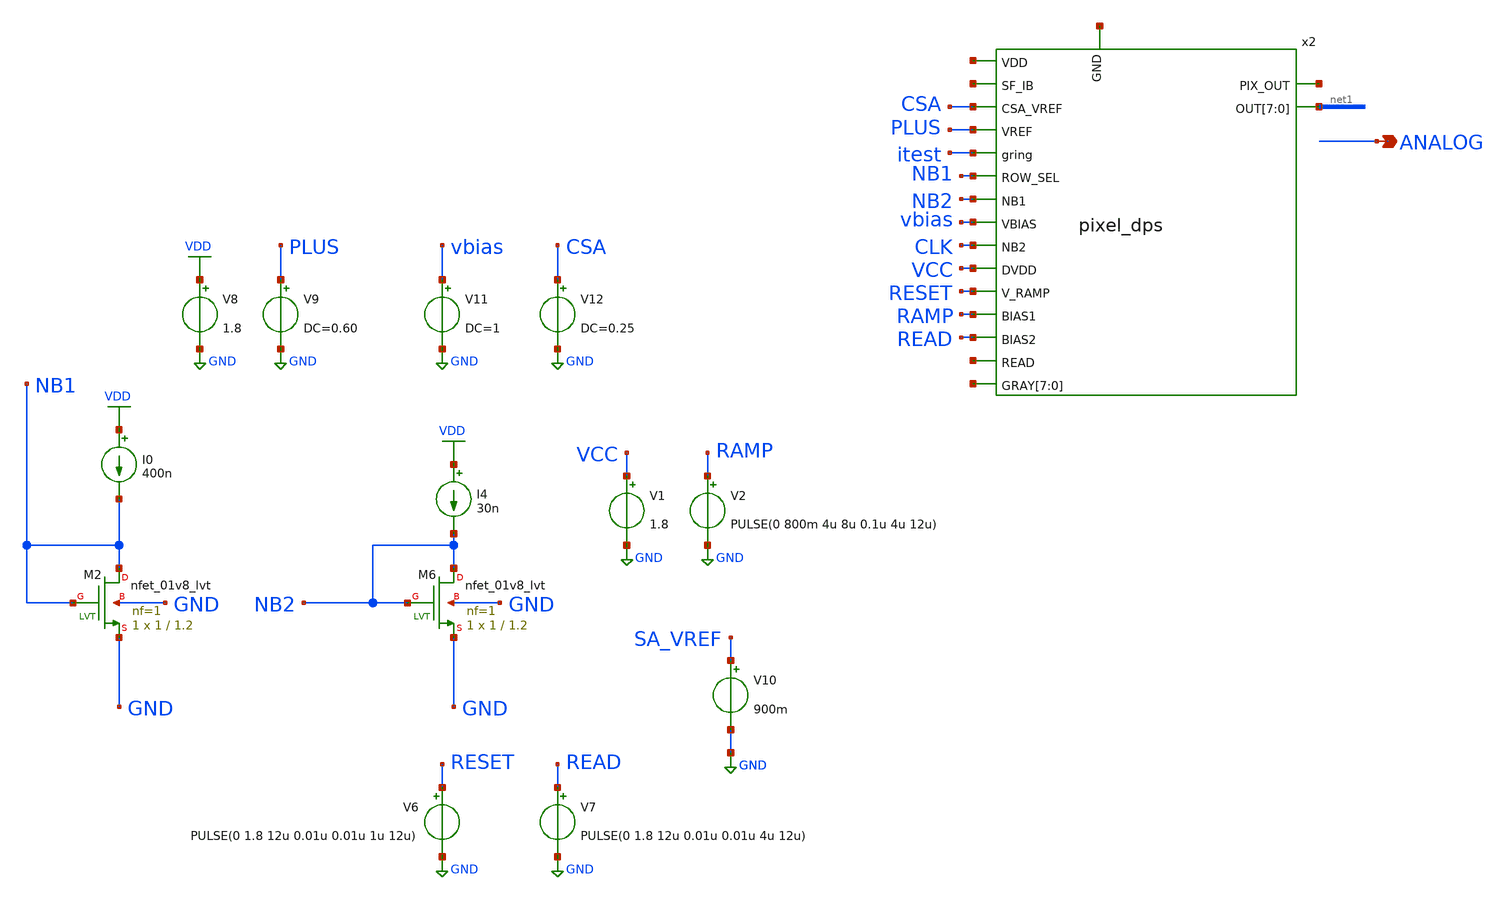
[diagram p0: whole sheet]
** sch_path: xschem/untitled-2.sch
**.subckt untitled-2 ANALOG
*.opin ANALOG
V8 VDD GND 1.8
V9 PLUS GND DC=0.60
V11 vbias GND DC=1
V12 CSA GND DC=0.25
V1 VCC GND 1.8
V2 RAMP GND PULSE(0 800m 4u 8u 0.1u 4u 12u)
XM2 NB1 NB1 GND GND sky130_fd_pr__nfet_01v8_lvt L=1.2 W=1 nf=1 ad='int((nf+1)/2) * W/nf * 0.29' as='int((nf+2)/2) * W/nf * 0.29'
+ pd='2*int((nf+1)/2) * (W/nf + 0.29)' ps='2*int((nf+2)/2) * (W/nf + 0.29)' nrd='0.29 / W' nrs='0.29 / W'
+ sa=0 sb=0 sd=0 mult=1 m=1
I0 VDD NB1 400n
I4 VDD NB2 30n
XM6 NB2 NB2 GND GND sky130_fd_pr__nfet_01v8_lvt L=1.2 W=1 nf=1 ad='int((nf+1)/2) * W/nf * 0.29' as='int((nf+2)/2) * W/nf * 0.29'
+ pd='2*int((nf+1)/2) * (W/nf + 0.29)' ps='2*int((nf+2)/2) * (W/nf + 0.29)' nrd='0.29 / W' nrs='0.29 / W'
+ sa=0 sb=0 sd=0 mult=1 m=1
V7 READ GND PULSE(0 1.8 12u 0.01u 0.01u 4u 12u)
V6 RESET GND PULSE(0 1.8 12u 0.01u 0.01u 1u 12u)
V10 SA_VREF GND 900m
x2 net2 net3 CSA PLUS net4 itest NB1 NB2 vbias CLK net1[7] net1[6] net1[5] net1[4] net1[3] net1[2]
+ net1[1] net1[0] VCC RESET RAMP READ net5 net6[7] net6[6] net6[5] net6[4] net6[3] net6[2] net6[1] net6[0]
+ net7 pixel_dps
**.ends
.GLOBAL GND
.GLOBAL VDD
.end
